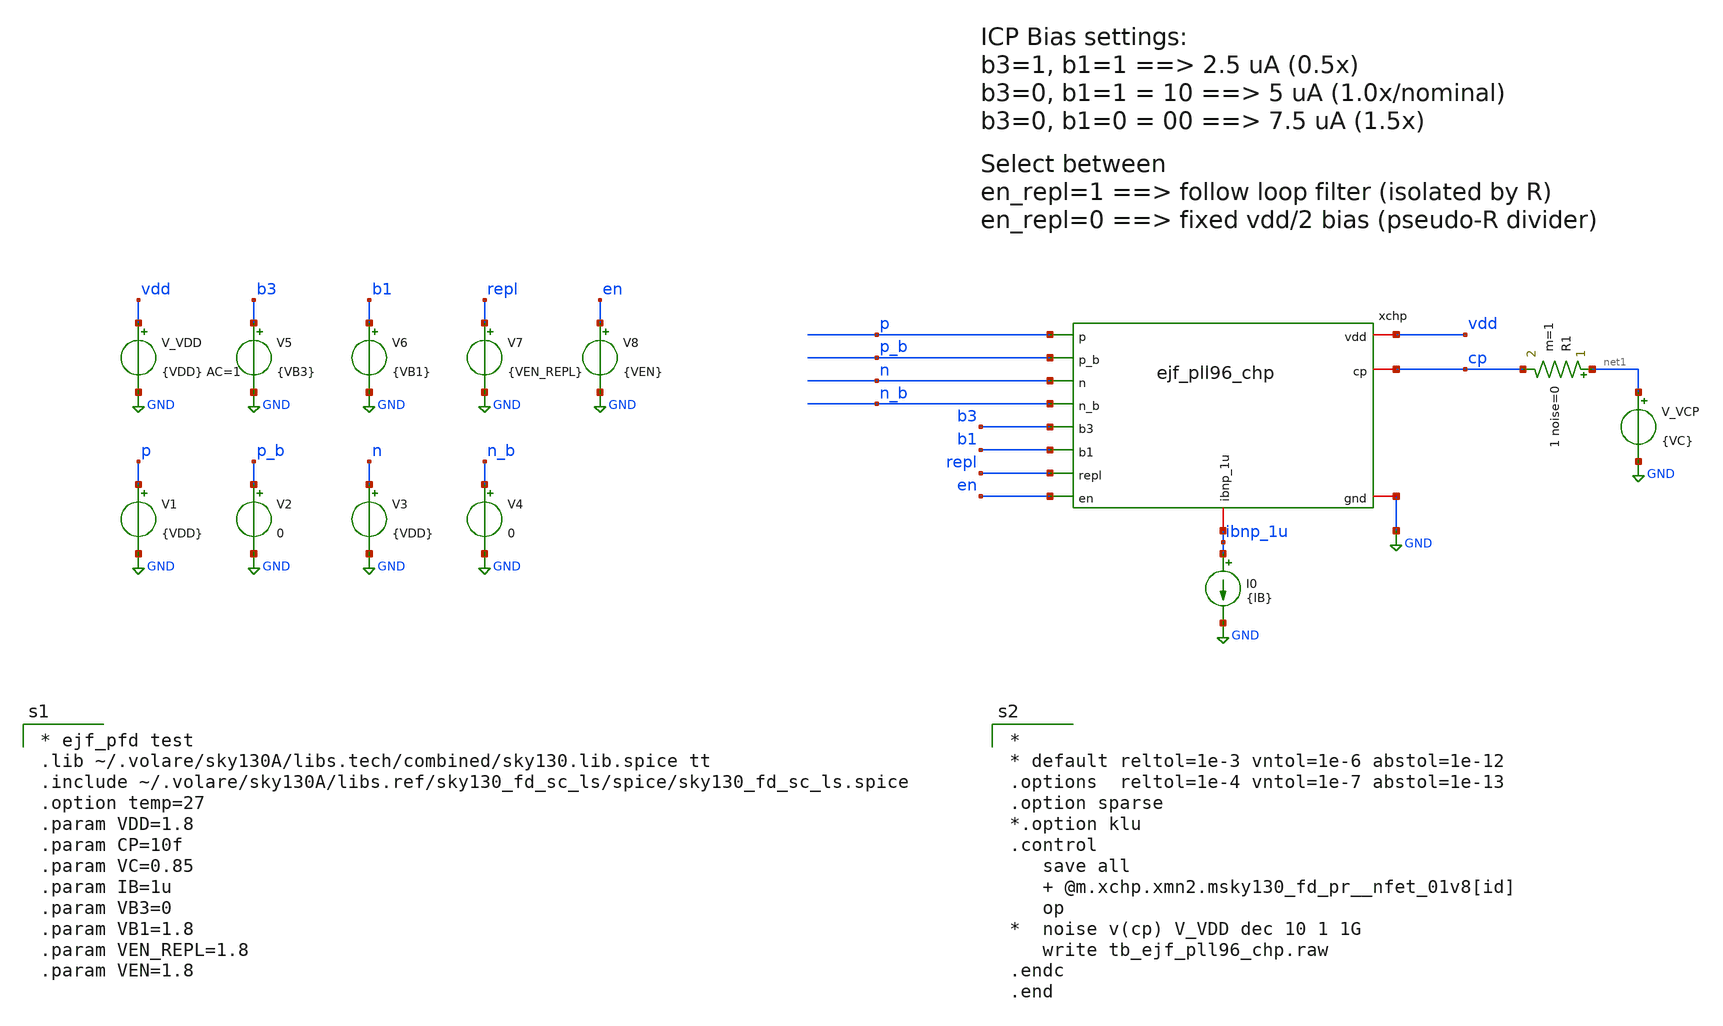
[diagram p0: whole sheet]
** sch_path: xschem/tb_ejf_pll96_chp.sch
**.subckt tb_ejf_pll96_chp
V_VDD vdd GND {VDD} AC=1
.save i(v_vdd)
xchp vdd p ibnp_1u p_b cp n_b n GND b3 b1 repl en ejf_pll96_chp
I0 ibnp_1u GND {IB}
V_VCP net1 GND {VC}
.save i(v_vcp)
V1 p GND {VDD}
.save i(v1)
V2 p_b GND 0
.save i(v2)
V3 n GND {VDD}
.save i(v3)
V4 n_b GND 0
.save i(v4)
R1 net1 cp 1 noise=0 m=1
V5 b3 GND {VB3}
.save i(v5)
V6 b1 GND {VB1}
.save i(v6)
V7 repl GND {VEN_REPL}
.save i(v7)
V8 en GND {VEN}
.save i(v8)
**** begin user architecture code

* ejf_pfd test
.lib ~/.volare/sky130A/libs.tech/combined/sky130.lib.spice tt
.include ~/.volare/sky130A/libs.ref/sky130_fd_sc_ls/spice/sky130_fd_sc_ls.spice
.option temp=27
.param VDD=1.8
.param CP=10f
.param VC=0.85
.param IB=1u
.param VB3=0
.param VB1=1.8
.param VEN_REPL=1.8
.param VEN=1.8



*
* default reltol=1e-3 vntol=1e-6 abstol=1e-12
.options  reltol=1e-4 vntol=1e-7 abstol=1e-13
.option sparse
*.option klu
.control
   save all
   + @m.xchp.xmn2.msky130_fd_pr__nfet_01v8[id]
   op
*  noise v(cp) V_VDD dec 10 1 1G
   write tb_ejf_pll96_chp.raw
.endc
.end

**** end user architecture code
**.ends

* expanding   symbol:  ejf_pll96_chp.sym # of pins=12
** sym_path: xschem/ejf_pll96_chp.sym
** sch_path: xschem/ejf_pll96_chp.sch
.subckt ejf_pll96_chp vdd p ibnp_1u p_b cp n_b n gnd b3 b1 repl en
*.iopin vdd
*.iopin gnd
*.iopin ibnp_1u
*.iopin cp
*.ipin p
*.ipin n_b
*.ipin p_b
*.ipin n
*.ipin en
*.ipin b3
*.ipin b1
*.ipin repl
XMP2_2 mp2d mp1g vdd vdd sky130_fd_pr__pfet_01v8_lvt L=1.2 W=1.2 nf=2 ad='int((nf+1)/2) * W/nf * 0.29'
+ as='int((nf+2)/2) * W/nf * 0.29' pd='2*int((nf+1)/2) * (W/nf + 0.29)' ps='2*int((nf+2)/2) * (W/nf + 0.29)'
+ nrd='0.29 / W' nrs='0.29 / W' sa=0 sb=0 sd=0 mult=1 m=1
XMN2 net1 mn1g gnd gnd sky130_fd_pr__nfet_01v8 L=1.2 W=0.6 nf=1 ad='int((nf+1)/2) * W/nf * 0.29' as='int((nf+2)/2) * W/nf * 0.29'
+ pd='2*int((nf+1)/2) * (W/nf + 0.29)' ps='2*int((nf+2)/2) * (W/nf + 0.29)' nrd='0.29 / W' nrs='0.29 / W'
+ sa=0 sb=0 sd=0 mult=1 m=1
XMN2C mn1g mn1cg net1 gnd sky130_fd_pr__nfet_01v8 L=0.3 W=0.6 nf=1 ad='int((nf+1)/2) * W/nf * 0.29' as='int((nf+2)/2) * W/nf * 0.29'
+ pd='2*int((nf+1)/2) * (W/nf + 0.29)' ps='2*int((nf+2)/2) * (W/nf + 0.29)' nrd='0.29 / W' nrs='0.29 / W'
+ sa=0 sb=0 sd=0 mult=1 m=1
XMP1 mp1d mp1g vdd vdd sky130_fd_pr__pfet_01v8_lvt L=1.2 W=1.8 nf=3 ad='int((nf+1)/2) * W/nf * 0.29'
+ as='int((nf+2)/2) * W/nf * 0.29' pd='2*int((nf+1)/2) * (W/nf + 0.29)' ps='2*int((nf+2)/2) * (W/nf + 0.29)'
+ nrd='0.29 / W' nrs='0.29 / W' sa=0 sb=0 sd=0 mult=5 m=5
XMP2C mp1g ibnp_1u mp2d vdd sky130_fd_pr__pfet_01v8_lvt L=0.35 W=1.2 nf=1 ad='int((nf+1)/2) * W/nf * 0.29'
+ as='int((nf+2)/2) * W/nf * 0.29' pd='2*int((nf+1)/2) * (W/nf + 0.29)' ps='2*int((nf+2)/2) * (W/nf + 0.29)'
+ nrd='0.29 / W' nrs='0.29 / W' sa=0 sb=0 sd=0 mult=1 m=1
XMP1C mp1cd ibnp_1u mp1d vdd sky130_fd_pr__pfet_01v8_lvt L=0.35 W=1.2 nf=1 ad='int((nf+1)/2) * W/nf * 0.29'
+ as='int((nf+2)/2) * W/nf * 0.29' pd='2*int((nf+1)/2) * (W/nf + 0.29)' ps='2*int((nf+2)/2) * (W/nf + 0.29)'
+ nrd='0.29 / W' nrs='0.29 / W' sa=0 sb=0 sd=0 mult=5 m=5
XMN1 mn1d mn1g gnd gnd sky130_fd_pr__nfet_01v8 L=1.2 W=0.6 nf=1 ad='int((nf+1)/2) * W/nf * 0.29' as='int((nf+2)/2) * W/nf * 0.29'
+ pd='2*int((nf+1)/2) * (W/nf + 0.29)' ps='2*int((nf+2)/2) * (W/nf + 0.29)' nrd='0.29 / W' nrs='0.29 / W'
+ sa=0 sb=0 sd=0 mult=5 m=5
XM1C mn1cd mn1cg mn1d gnd sky130_fd_pr__nfet_01v8 L=0.3 W=0.6 nf=1 ad='int((nf+1)/2) * W/nf * 0.29' as='int((nf+2)/2) * W/nf * 0.29'
+ pd='2*int((nf+1)/2) * (W/nf + 0.29)' ps='2*int((nf+2)/2) * (W/nf + 0.29)' nrd='0.29 / W' nrs='0.29 / W'
+ sa=0 sb=0 sd=0 mult=5 m=5
XMP11 cp_repl p mp1cd vdd sky130_fd_pr__pfet_01v8 L=0.15 W=1 nf=1 ad='int((nf+1)/2) * W/nf * 0.29' as='int((nf+2)/2) * W/nf * 0.29'
+ pd='2*int((nf+1)/2) * (W/nf + 0.29)' ps='2*int((nf+2)/2) * (W/nf + 0.29)' nrd='0.29 / W' nrs='0.29 / W'
+ sa=0 sb=0 sd=0 mult=1 m=1
XMN11 cp_repl n_b mn1cd gnd sky130_fd_pr__nfet_01v8 L=0.15 W=1 nf=1 ad='int((nf+1)/2) * W/nf * 0.29'
+ as='int((nf+2)/2) * W/nf * 0.29' pd='2*int((nf+1)/2) * (W/nf + 0.29)' ps='2*int((nf+2)/2) * (W/nf + 0.29)'
+ nrd='0.29 / W' nrs='0.29 / W' sa=0 sb=0 sd=0 mult=1 m=1
XMP10 cp p_b mp1cd vdd sky130_fd_pr__pfet_01v8 L=0.15 W=1 nf=1 ad='int((nf+1)/2) * W/nf * 0.29' as='int((nf+2)/2) * W/nf * 0.29'
+ pd='2*int((nf+1)/2) * (W/nf + 0.29)' ps='2*int((nf+2)/2) * (W/nf + 0.29)' nrd='0.29 / W' nrs='0.29 / W'
+ sa=0 sb=0 sd=0 mult=1 m=1
XMN10 cp n mn1cd gnd sky130_fd_pr__nfet_01v8 L=0.15 W=1 nf=1 ad='int((nf+1)/2) * W/nf * 0.29' as='int((nf+2)/2) * W/nf * 0.29'
+ pd='2*int((nf+1)/2) * (W/nf + 0.29)' ps='2*int((nf+2)/2) * (W/nf + 0.29)' nrd='0.29 / W' nrs='0.29 / W'
+ sa=0 sb=0 sd=0 mult=1 m=1
XMN4CAP gnd mn1g gnd gnd sky130_fd_pr__nfet_01v8 L=1.2 W=0.6 nf=1 ad='int((nf+1)/2) * W/nf * 0.29' as='int((nf+2)/2) * W/nf * 0.29'
+ pd='2*int((nf+1)/2) * (W/nf + 0.29)' ps='2*int((nf+2)/2) * (W/nf + 0.29)' nrd='0.29 / W' nrs='0.29 / W'
+ sa=0 sb=0 sd=0 mult=11 m=11
XMP4CAP vdd mp1g vdd vdd sky130_fd_pr__pfet_01v8_lvt L=1.2 W=1.8 nf=3 ad='int((nf+1)/2) * W/nf * 0.29'
+ as='int((nf+2)/2) * W/nf * 0.29' pd='2*int((nf+1)/2) * (W/nf + 0.29)' ps='2*int((nf+2)/2) * (W/nf + 0.29)'
+ nrd='0.29 / W' nrs='0.29 / W' sa=0 sb=0 sd=0 mult=13 m=13
XMP5CAP vdd ibnp_1u vdd vdd sky130_fd_pr__pfet_01v8_lvt L=1.2 W=1.8 nf=3 ad='int((nf+1)/2) * W/nf * 0.29'
+ as='int((nf+2)/2) * W/nf * 0.29' pd='2*int((nf+1)/2) * (W/nf + 0.29)' ps='2*int((nf+2)/2) * (W/nf + 0.29)'
+ nrd='0.29 / W' nrs='0.29 / W' sa=0 sb=0 sd=0 mult=13 m=13
XMN5CAP gnd mn1cg gnd gnd sky130_fd_pr__nfet_01v8 L=1.2 W=0.6 nf=1 ad='int((nf+1)/2) * W/nf * 0.29' as='int((nf+2)/2) * W/nf * 0.29'
+ pd='2*int((nf+1)/2) * (W/nf + 0.29)' ps='2*int((nf+2)/2) * (W/nf + 0.29)' nrd='0.29 / W' nrs='0.29 / W'
+ sa=0 sb=0 sd=0 mult=11 m=11
XMP20 mp20d mp1g vdd vdd sky130_fd_pr__pfet_01v8_lvt L=1.2 W=1.8 nf=3 ad='int((nf+1)/2) * W/nf * 0.29'
+ as='int((nf+2)/2) * W/nf * 0.29' pd='2*int((nf+1)/2) * (W/nf + 0.29)' ps='2*int((nf+2)/2) * (W/nf + 0.29)'
+ nrd='0.29 / W' nrs='0.29 / W' sa=0 sb=0 sd=0 mult=5 m=5
XMN6 mp21cg mn1g gnd gnd sky130_fd_pr__nfet_01v8 L=1.2 W=0.6 nf=1 ad='int((nf+1)/2) * W/nf * 0.29' as='int((nf+2)/2) * W/nf * 0.29'
+ pd='2*int((nf+1)/2) * (W/nf + 0.29)' ps='2*int((nf+2)/2) * (W/nf + 0.29)' nrd='0.29 / W' nrs='0.29 / W'
+ sa=0 sb=0 sd=0 mult=1 m=1
XMPC1 vdd cp_repl vdd vdd sky130_fd_pr__pfet_01v8_lvt L=7.5 W=60 nf=10 ad='int((nf+1)/2) * W/nf * 0.29'
+ as='int((nf+2)/2) * W/nf * 0.29' pd='2*int((nf+1)/2) * (W/nf + 0.29)' ps='2*int((nf+2)/2) * (W/nf + 0.29)'
+ nrd='0.29 / W' nrs='0.29 / W' sa=0 sb=0 sd=0 mult=1 m=1
XM12 mn1cg en_b gnd gnd sky130_fd_pr__nfet_01v8 L=0.15 W=1 nf=1 ad='int((nf+1)/2) * W/nf * 0.29' as='int((nf+2)/2) * W/nf * 0.29'
+ pd='2*int((nf+1)/2) * (W/nf + 0.29)' ps='2*int((nf+2)/2) * (W/nf + 0.29)' nrd='0.29 / W' nrs='0.29 / W'
+ sa=0 sb=0 sd=0 mult=1 m=1
XM13 mn1g en_b gnd gnd sky130_fd_pr__nfet_01v8 L=0.15 W=1 nf=1 ad='int((nf+1)/2) * W/nf * 0.29' as='int((nf+2)/2) * W/nf * 0.29'
+ pd='2*int((nf+1)/2) * (W/nf + 0.29)' ps='2*int((nf+2)/2) * (W/nf + 0.29)' nrd='0.29 / W' nrs='0.29 / W'
+ sa=0 sb=0 sd=0 mult=1 m=1
XMP21P net3 amp_inp mp20d vdd sky130_fd_pr__pfet_01v8_lvt L=0.35 W=1.2 nf=1 ad='int((nf+1)/2) * W/nf * 0.29'
+ as='int((nf+2)/2) * W/nf * 0.29' pd='2*int((nf+1)/2) * (W/nf + 0.29)' ps='2*int((nf+2)/2) * (W/nf + 0.29)'
+ nrd='0.29 / W' nrs='0.29 / W' sa=0 sb=0 sd=0 mult=1 m=1
XMP21N net4 cp_repl mp20d vdd sky130_fd_pr__pfet_01v8_lvt L=0.35 W=1.2 nf=1 ad='int((nf+1)/2) * W/nf * 0.29'
+ as='int((nf+2)/2) * W/nf * 0.29' pd='2*int((nf+1)/2) * (W/nf + 0.29)' ps='2*int((nf+2)/2) * (W/nf + 0.29)'
+ nrd='0.29 / W' nrs='0.29 / W' sa=0 sb=0 sd=0 mult=1 m=1
XMP24 mp21cg mp21cg mp20d vdd sky130_fd_pr__pfet_01v8_lvt L=2.8 W=1.2 nf=1 ad='int((nf+1)/2) * W/nf * 0.29'
+ as='int((nf+2)/2) * W/nf * 0.29' pd='2*int((nf+1)/2) * (W/nf + 0.29)' ps='2*int((nf+2)/2) * (W/nf + 0.29)'
+ nrd='0.29 / W' nrs='0.29 / W' sa=0 sb=0 sd=0 mult=1 m=1
XMP21NC cp_repl mp21cg net4 vdd sky130_fd_pr__pfet_01v8_lvt L=0.35 W=1.2 nf=1 ad='int((nf+1)/2) * W/nf * 0.29'
+ as='int((nf+2)/2) * W/nf * 0.29' pd='2*int((nf+1)/2) * (W/nf + 0.29)' ps='2*int((nf+2)/2) * (W/nf + 0.29)'
+ nrd='0.29 / W' nrs='0.29 / W' sa=0 sb=0 sd=0 mult=1 m=1
XMP21PC net2 mp21cg net3 vdd sky130_fd_pr__pfet_01v8_lvt L=0.35 W=1.2 nf=1 ad='int((nf+1)/2) * W/nf * 0.29'
+ as='int((nf+2)/2) * W/nf * 0.29' pd='2*int((nf+1)/2) * (W/nf + 0.29)' ps='2*int((nf+2)/2) * (W/nf + 0.29)'
+ nrd='0.29 / W' nrs='0.29 / W' sa=0 sb=0 sd=0 mult=1 m=1
XMN24 net6 net2 gnd gnd sky130_fd_pr__nfet_01v8 L=1.2 W=0.6 nf=1 ad='int((nf+1)/2) * W/nf * 0.29' as='int((nf+2)/2) * W/nf * 0.29'
+ pd='2*int((nf+1)/2) * (W/nf + 0.29)' ps='2*int((nf+2)/2) * (W/nf + 0.29)' nrd='0.29 / W' nrs='0.29 / W'
+ sa=0 sb=0 sd=0 mult=2 m=2
XMN23 net5 net2 gnd gnd sky130_fd_pr__nfet_01v8 L=1.2 W=0.6 nf=1 ad='int((nf+1)/2) * W/nf * 0.29' as='int((nf+2)/2) * W/nf * 0.29'
+ pd='2*int((nf+1)/2) * (W/nf + 0.29)' ps='2*int((nf+2)/2) * (W/nf + 0.29)' nrd='0.29 / W' nrs='0.29 / W'
+ sa=0 sb=0 sd=0 mult=2 m=2
XMN24C net2 mn1cg net6 gnd sky130_fd_pr__nfet_01v8 L=0.3 W=0.6 nf=1 ad='int((nf+1)/2) * W/nf * 0.29'
+ as='int((nf+2)/2) * W/nf * 0.29' pd='2*int((nf+1)/2) * (W/nf + 0.29)' ps='2*int((nf+2)/2) * (W/nf + 0.29)'
+ nrd='0.29 / W' nrs='0.29 / W' sa=0 sb=0 sd=0 mult=2 m=2
XMN23C cp_repl mn1cg net5 gnd sky130_fd_pr__nfet_01v8 L=0.3 W=0.6 nf=1 ad='int((nf+1)/2) * W/nf * 0.29'
+ as='int((nf+2)/2) * W/nf * 0.29' pd='2*int((nf+1)/2) * (W/nf + 0.29)' ps='2*int((nf+2)/2) * (W/nf + 0.29)'
+ nrd='0.29 / W' nrs='0.29 / W' sa=0 sb=0 sd=0 mult=2 m=2
XM8 net9 repl_b gnd gnd sky130_fd_pr__nfet_01v8 L=0.15 W=1 nf=1 ad='int((nf+1)/2) * W/nf * 0.29' as='int((nf+2)/2) * W/nf * 0.29'
+ pd='2*int((nf+1)/2) * (W/nf + 0.29)' ps='2*int((nf+2)/2) * (W/nf + 0.29)' nrd='0.29 / W' nrs='0.29 / W'
+ sa=0 sb=0 sd=0 mult=1 m=1
XM5 net7 repl_bb vdd vdd sky130_fd_pr__pfet_01v8_hvt L=0.15 W=2 nf=1 ad='int((nf+1)/2) * W/nf * 0.29'
+ as='int((nf+2)/2) * W/nf * 0.29' pd='2*int((nf+1)/2) * (W/nf + 0.29)' ps='2*int((nf+2)/2) * (W/nf + 0.29)'
+ nrd='0.29 / W' nrs='0.29 / W' sa=0 sb=0 sd=0 mult=1 m=1
XM6 amp_inp net7 net7 net7 sky130_fd_pr__pfet_01v8_lvt L=0.35 W=40 nf=8 ad='int((nf+1)/2) * W/nf * 0.29'
+ as='int((nf+2)/2) * W/nf * 0.29' pd='2*int((nf+1)/2) * (W/nf + 0.29)' ps='2*int((nf+2)/2) * (W/nf + 0.29)'
+ nrd='0.29 / W' nrs='0.29 / W' sa=0 sb=0 sd=0 mult=1 m=1
XM7 net9 amp_inp amp_inp amp_inp sky130_fd_pr__pfet_01v8_lvt L=0.35 W=40 nf=8 ad='int((nf+1)/2) * W/nf * 0.29'
+ as='int((nf+2)/2) * W/nf * 0.29' pd='2*int((nf+1)/2) * (W/nf + 0.29)' ps='2*int((nf+2)/2) * (W/nf + 0.29)'
+ nrd='0.29 / W' nrs='0.29 / W' sa=0 sb=0 sd=0 mult=1 m=1
XMN4 net8 repl_bb amp_inp gnd sky130_fd_pr__nfet_01v8 L=0.15 W=1 nf=1 ad='int((nf+1)/2) * W/nf * 0.29'
+ as='int((nf+2)/2) * W/nf * 0.29' pd='2*int((nf+1)/2) * (W/nf + 0.29)' ps='2*int((nf+2)/2) * (W/nf + 0.29)'
+ nrd='0.29 / W' nrs='0.29 / W' sa=0 sb=0 sd=0 mult=1 m=1
XM9 net8 repl_b amp_inp vdd sky130_fd_pr__pfet_01v8_hvt L=0.15 W=2 nf=1 ad='int((nf+1)/2) * W/nf * 0.29'
+ as='int((nf+2)/2) * W/nf * 0.29' pd='2*int((nf+1)/2) * (W/nf + 0.29)' ps='2*int((nf+2)/2) * (W/nf + 0.29)'
+ nrd='0.29 / W' nrs='0.29 / W' sa=0 sb=0 sd=0 mult=1 m=1
XMP2_1 mp2d net10 vdd vdd sky130_fd_pr__pfet_01v8_lvt L=1.2 W=0.6 nf=1 ad='int((nf+1)/2) * W/nf * 0.29'
+ as='int((nf+2)/2) * W/nf * 0.29' pd='2*int((nf+1)/2) * (W/nf + 0.29)' ps='2*int((nf+2)/2) * (W/nf + 0.29)'
+ nrd='0.29 / W' nrs='0.29 / W' sa=0 sb=0 sd=0 mult=1 m=1
XMP2_3 mp2d net11 vdd vdd sky130_fd_pr__pfet_01v8_lvt L=1.2 W=1.8 nf=3 ad='int((nf+1)/2) * W/nf * 0.29'
+ as='int((nf+2)/2) * W/nf * 0.29' pd='2*int((nf+1)/2) * (W/nf + 0.29)' ps='2*int((nf+2)/2) * (W/nf + 0.29)'
+ nrd='0.29 / W' nrs='0.29 / W' sa=0 sb=0 sd=0 mult=1 m=1
XM4 net11 b3_bb vdd vdd sky130_fd_pr__pfet_01v8_hvt L=0.15 W=2 nf=1 ad='int((nf+1)/2) * W/nf * 0.29'
+ as='int((nf+2)/2) * W/nf * 0.29' pd='2*int((nf+1)/2) * (W/nf + 0.29)' ps='2*int((nf+2)/2) * (W/nf + 0.29)'
+ nrd='0.29 / W' nrs='0.29 / W' sa=0 sb=0 sd=0 mult=1 m=1
XMP3C mn1cg ibnp_1u net12 vdd sky130_fd_pr__pfet_01v8_lvt L=0.35 W=1.2 nf=1 ad='int((nf+1)/2) * W/nf * 0.29'
+ as='int((nf+2)/2) * W/nf * 0.29' pd='2*int((nf+1)/2) * (W/nf + 0.29)' ps='2*int((nf+2)/2) * (W/nf + 0.29)'
+ nrd='0.29 / W' nrs='0.29 / W' sa=0 sb=0 sd=0 mult=1 m=1
XMP3 net12 mp1g vdd vdd sky130_fd_pr__pfet_01v8_lvt L=1.2 W=1.8 nf=3 ad='int((nf+1)/2) * W/nf * 0.29'
+ as='int((nf+2)/2) * W/nf * 0.29' pd='2*int((nf+1)/2) * (W/nf + 0.29)' ps='2*int((nf+2)/2) * (W/nf + 0.29)'
+ nrd='0.29 / W' nrs='0.29 / W' sa=0 sb=0 sd=0 mult=1 m=1
x1 vdd en en_bb en_b gnd ejf_pll96_dbuf
x2 vdd repl repl_bb repl_b gnd ejf_pll96_dbuf
x3 vdd b3 b3_bb b3_b gnd ejf_pll96_dbuf
x4 vdd b1 b1_bb b1_b gnd ejf_pll96_dbuf
XM1 mp1g b3_b net11 vdd sky130_fd_pr__pfet_01v8_hvt L=0.15 W=2 nf=1 ad='int((nf+1)/2) * W/nf * 0.29'
+ as='int((nf+2)/2) * W/nf * 0.29' pd='2*int((nf+1)/2) * (W/nf + 0.29)' ps='2*int((nf+2)/2) * (W/nf + 0.29)'
+ nrd='0.29 / W' nrs='0.29 / W' sa=0 sb=0 sd=0 mult=1 m=1
XM2 net10 b1_bb vdd vdd sky130_fd_pr__pfet_01v8_hvt L=0.15 W=2 nf=1 ad='int((nf+1)/2) * W/nf * 0.29'
+ as='int((nf+2)/2) * W/nf * 0.29' pd='2*int((nf+1)/2) * (W/nf + 0.29)' ps='2*int((nf+2)/2) * (W/nf + 0.29)'
+ nrd='0.29 / W' nrs='0.29 / W' sa=0 sb=0 sd=0 mult=1 m=1
XM3 mp1g b1_b net10 vdd sky130_fd_pr__pfet_01v8_hvt L=0.15 W=2 nf=1 ad='int((nf+1)/2) * W/nf * 0.29'
+ as='int((nf+2)/2) * W/nf * 0.29' pd='2*int((nf+1)/2) * (W/nf + 0.29)' ps='2*int((nf+2)/2) * (W/nf + 0.29)'
+ nrd='0.29 / W' nrs='0.29 / W' sa=0 sb=0 sd=0 mult=1 m=1
XM10 ibnp_1u en_bb vdd vdd sky130_fd_pr__pfet_01v8_hvt L=0.15 W=2 nf=1 ad='int((nf+1)/2) * W/nf * 0.29'
+ as='int((nf+2)/2) * W/nf * 0.29' pd='2*int((nf+1)/2) * (W/nf + 0.29)' ps='2*int((nf+2)/2) * (W/nf + 0.29)'
+ nrd='0.29 / W' nrs='0.29 / W' sa=0 sb=0 sd=0 mult=1 m=1
XM11 mp1g en_bb vdd vdd sky130_fd_pr__pfet_01v8_hvt L=0.15 W=2 nf=1 ad='int((nf+1)/2) * W/nf * 0.29'
+ as='int((nf+2)/2) * W/nf * 0.29' pd='2*int((nf+1)/2) * (W/nf + 0.29)' ps='2*int((nf+2)/2) * (W/nf + 0.29)'
+ nrd='0.29 / W' nrs='0.29 / W' sa=0 sb=0 sd=0 mult=1 m=1
XR1 net15 net16 vdd sky130_fd_pr__res_high_po_0p35 L=23 mult=1 m=1
XR2 ibnp_1u net15 vdd sky130_fd_pr__res_high_po_0p35 L=23 mult=1 m=1
XR3 net14 mp1g vdd sky130_fd_pr__res_high_po_0p35 L=23 mult=1 m=1
XR4 net16 net14 vdd sky130_fd_pr__res_high_po_0p35 L=23 mult=1 m=1
XR5[1] vdd vdd vdd sky130_fd_pr__res_high_po_0p35 L=23 mult=1 m=1
XR5[0] vdd vdd vdd sky130_fd_pr__res_high_po_0p35 L=23 mult=1 m=1
XR5 net13 net18 gnd sky130_fd_pr__res_high_po_0p35 L=23 mult=1 m=1
XR6 net19 net13 gnd sky130_fd_pr__res_high_po_0p35 L=23 mult=1 m=1
XR7 net20 net19 gnd sky130_fd_pr__res_high_po_0p35 L=23 mult=1 m=1
XR8 mn1g net20 gnd sky130_fd_pr__res_high_po_0p35 L=23 mult=1 m=1
XR9 net17 mn1cg gnd sky130_fd_pr__res_high_po_0p35 L=23 mult=1 m=1
XR10 net21 net17 gnd sky130_fd_pr__res_high_po_0p35 L=23 mult=1 m=1
XR11 net22 net21 gnd sky130_fd_pr__res_high_po_0p35 L=23 mult=1 m=1
XR12 net18 net22 gnd sky130_fd_pr__res_high_po_0p35 L=23 mult=1 m=1
XR13[1] gnd gnd gnd sky130_fd_pr__res_high_po_0p35 L=23 mult=1 m=1
XR13[0] gnd gnd gnd sky130_fd_pr__res_high_po_0p35 L=23 mult=1 m=1
XR13 net23 net8 vdd sky130_fd_pr__res_high_po_0p35 L=23 mult=1 m=1
XR14 cp net23 vdd sky130_fd_pr__res_high_po_0p35 L=23 mult=1 m=1
XR15[1] vdd vdd vdd sky130_fd_pr__res_high_po_0p35 L=23 mult=1 m=1
XR15[0] vdd vdd vdd sky130_fd_pr__res_high_po_0p35 L=23 mult=1 m=1
.ends


* expanding   symbol:  ejf_pll96_dbuf.sym # of pins=5
** sym_path: xschem/ejf_pll96_dbuf.sym
** sch_path: xschem/ejf_pll96_dbuf.sch
.subckt ejf_pll96_dbuf vdd a y y_b gnd
*.ipin a
*.iopin vdd
*.iopin gnd
*.opin y
*.opin y_b
XMP1 y_b a vdd vdd sky130_fd_pr__pfet_01v8_hvt L=0.15 W=2 nf=1 ad='int((nf+1)/2) * W/nf * 0.29' as='int((nf+2)/2) * W/nf * 0.29'
+ pd='2*int((nf+1)/2) * (W/nf + 0.29)' ps='2*int((nf+2)/2) * (W/nf + 0.29)' nrd='0.29 / W' nrs='0.29 / W'
+ sa=0 sb=0 sd=0 mult=1 m=1
XMP3 y y_b vdd vdd sky130_fd_pr__pfet_01v8_hvt L=0.15 W=2 nf=1 ad='int((nf+1)/2) * W/nf * 0.29' as='int((nf+2)/2) * W/nf * 0.29'
+ pd='2*int((nf+1)/2) * (W/nf + 0.29)' ps='2*int((nf+2)/2) * (W/nf + 0.29)' nrd='0.29 / W' nrs='0.29 / W'
+ sa=0 sb=0 sd=0 mult=1 m=1
XMN4 y y_b gnd gnd sky130_fd_pr__nfet_01v8 L=0.15 W=1 nf=1 ad='int((nf+1)/2) * W/nf * 0.29' as='int((nf+2)/2) * W/nf * 0.29'
+ pd='2*int((nf+1)/2) * (W/nf + 0.29)' ps='2*int((nf+2)/2) * (W/nf + 0.29)' nrd='0.29 / W' nrs='0.29 / W'
+ sa=0 sb=0 sd=0 mult=1 m=1
XMN2 y_b a gnd gnd sky130_fd_pr__nfet_01v8 L=0.15 W=1 nf=1 ad='int((nf+1)/2) * W/nf * 0.29' as='int((nf+2)/2) * W/nf * 0.29'
+ pd='2*int((nf+1)/2) * (W/nf + 0.29)' ps='2*int((nf+2)/2) * (W/nf + 0.29)' nrd='0.29 / W' nrs='0.29 / W'
+ sa=0 sb=0 sd=0 mult=1 m=1
.ends

.GLOBAL GND
.end
